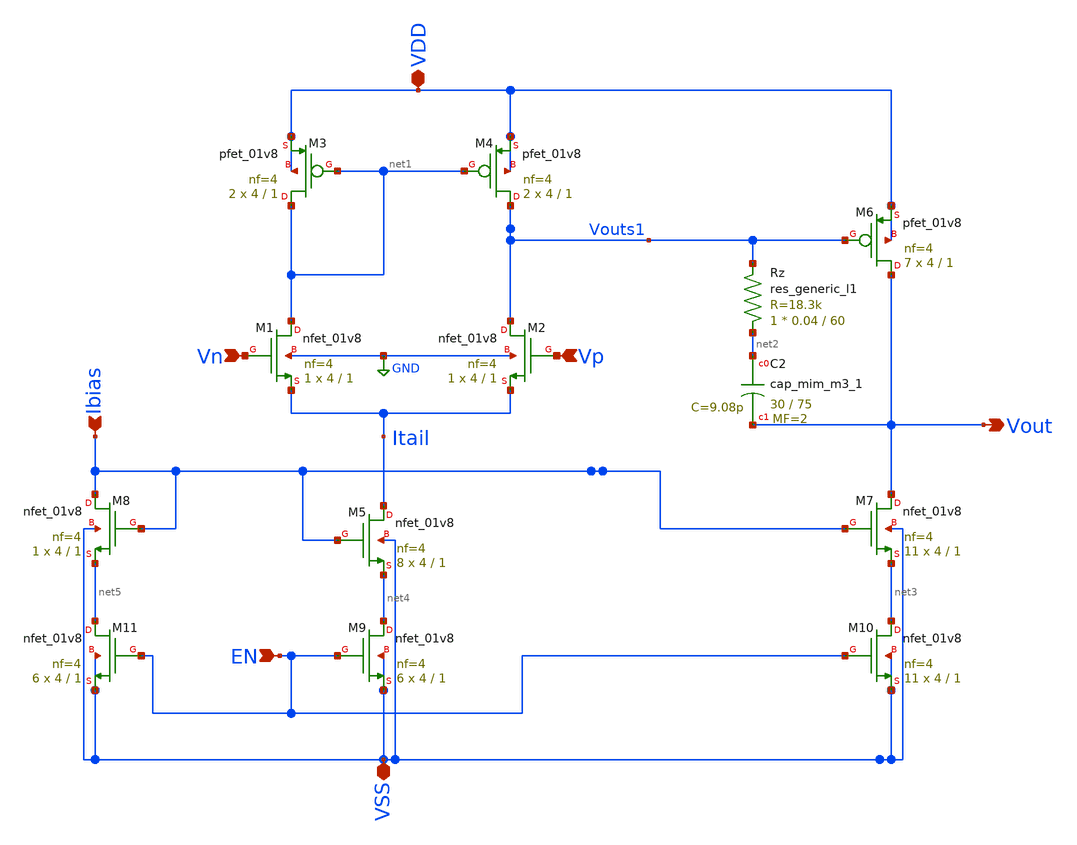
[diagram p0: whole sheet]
** sch_path: xschem/Opamp.sch
**.subckt Opamp Vn Ibias Vp EN Vout VSS VDD
*.ipin Vn
*.ipin Ibias
*.ipin Vp
*.ipin EN
*.opin Vout
*.iopin VSS
*.iopin VDD
XM2 Vouts1 Vp Itail GND sky130_fd_pr__nfet_01v8 L=1 W=4 nf=4 ad='int((nf+1)/2) * W/nf * 0.29' as='int((nf+2)/2) * W/nf * 0.29'
+ pd='2*int((nf+1)/2) * (W/nf + 0.29)' ps='2*int((nf+2)/2) * (W/nf + 0.29)' nrd='0.29 / W' nrs='0.29 / W'
+ sa=0 sb=0 sd=0 mult=1 m=1
XM4 Vouts1 net1 VDD VDD sky130_fd_pr__pfet_01v8 L=1 W=4 nf=4 ad='int((nf+1)/2) * W/nf * 0.29' as='int((nf+2)/2) * W/nf * 0.29'
+ pd='2*int((nf+1)/2) * (W/nf + 0.29)' ps='2*int((nf+2)/2) * (W/nf + 0.29)' nrd='0.29 / W' nrs='0.29 / W'
+ sa=0 sb=0 sd=0 mult=2 m=2
XM3 net1 net1 VDD VDD sky130_fd_pr__pfet_01v8 L=1 W=4 nf=4 ad='int((nf+1)/2) * W/nf * 0.29' as='int((nf+2)/2) * W/nf * 0.29'
+ pd='2*int((nf+1)/2) * (W/nf + 0.29)' ps='2*int((nf+2)/2) * (W/nf + 0.29)' nrd='0.29 / W' nrs='0.29 / W'
+ sa=0 sb=0 sd=0 mult=2 m=2
XM1 net1 Vn Itail GND sky130_fd_pr__nfet_01v8 L=1 W=4 nf=4 ad='int((nf+1)/2) * W/nf * 0.29' as='int((nf+2)/2) * W/nf * 0.29'
+ pd='2*int((nf+1)/2) * (W/nf + 0.29)' ps='2*int((nf+2)/2) * (W/nf + 0.29)' nrd='0.29 / W' nrs='0.29 / W'
+ sa=0 sb=0 sd=0 mult=1 m=1
XM6 Vout Vouts1 VDD VDD sky130_fd_pr__pfet_01v8 L=1 W=4 nf=4 ad='int((nf+1)/2) * W/nf * 0.29' as='int((nf+2)/2) * W/nf * 0.29'
+ pd='2*int((nf+1)/2) * (W/nf + 0.29)' ps='2*int((nf+2)/2) * (W/nf + 0.29)' nrd='0.29 / W' nrs='0.29 / W'
+ sa=0 sb=0 sd=0 mult=7 m=7
XM5 Itail Ibias net4 VSS sky130_fd_pr__nfet_01v8 L=1 W=4 nf=4 ad='int((nf+1)/2) * W/nf * 0.29' as='int((nf+2)/2) * W/nf * 0.29'
+ pd='2*int((nf+1)/2) * (W/nf + 0.29)' ps='2*int((nf+2)/2) * (W/nf + 0.29)' nrd='0.29 / W' nrs='0.29 / W'
+ sa=0 sb=0 sd=0 mult=8 m=8
XM7 Vout Ibias net3 VSS sky130_fd_pr__nfet_01v8 L=1 W=4 nf=4 ad='int((nf+1)/2) * W/nf * 0.29' as='int((nf+2)/2) * W/nf * 0.29'
+ pd='2*int((nf+1)/2) * (W/nf + 0.29)' ps='2*int((nf+2)/2) * (W/nf + 0.29)' nrd='0.29 / W' nrs='0.29 / W'
+ sa=0 sb=0 sd=0 mult=11 m=11
XM8 Ibias Ibias net5 VSS sky130_fd_pr__nfet_01v8 L=1 W=4 nf=4 ad='int((nf+1)/2) * W/nf * 0.29' as='int((nf+2)/2) * W/nf * 0.29'
+ pd='2*int((nf+1)/2) * (W/nf + 0.29)' ps='2*int((nf+2)/2) * (W/nf + 0.29)' nrd='0.29 / W' nrs='0.29 / W'
+ sa=0 sb=0 sd=0 mult=1 m=1
XC2 net2 Vout sky130_fd_pr__cap_mim_m3_1 W=30 L=75 MF=2 m=2
Rz net2 Vouts1 sky130_fd_pr__res_generic_l1 W=0.04 L=60 m=1
XM9 net4 EN VSS VSS sky130_fd_pr__nfet_01v8 L=1 W=4 nf=4 ad='int((nf+1)/2) * W/nf * 0.29' as='int((nf+2)/2) * W/nf * 0.29'
+ pd='2*int((nf+1)/2) * (W/nf + 0.29)' ps='2*int((nf+2)/2) * (W/nf + 0.29)' nrd='0.29 / W' nrs='0.29 / W'
+ sa=0 sb=0 sd=0 mult=6 m=6
XM10 net3 EN VSS VSS sky130_fd_pr__nfet_01v8 L=1 W=4 nf=4 ad='int((nf+1)/2) * W/nf * 0.29' as='int((nf+2)/2) * W/nf * 0.29'
+ pd='2*int((nf+1)/2) * (W/nf + 0.29)' ps='2*int((nf+2)/2) * (W/nf + 0.29)' nrd='0.29 / W' nrs='0.29 / W'
+ sa=0 sb=0 sd=0 mult=11 m=11
XM11 net5 EN VSS VSS sky130_fd_pr__nfet_01v8 L=1 W=4 nf=4 ad='int((nf+1)/2) * W/nf * 0.29' as='int((nf+2)/2) * W/nf * 0.29'
+ pd='2*int((nf+1)/2) * (W/nf + 0.29)' ps='2*int((nf+2)/2) * (W/nf + 0.29)' nrd='0.29 / W' nrs='0.29 / W'
+ sa=0 sb=0 sd=0 mult=6 m=6
**** begin user architecture code
"Is Subcircuit" = YES
**** end user architecture code
**.ends
.GLOBAL GND
.end
